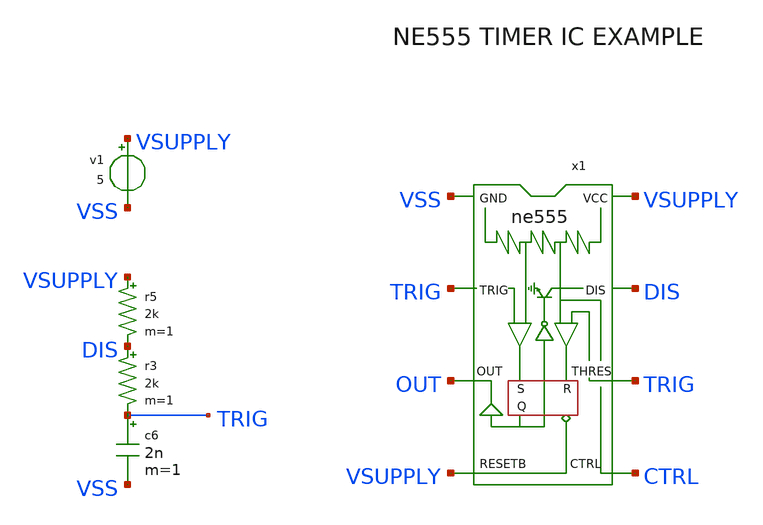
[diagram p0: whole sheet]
** sch_path: library/examples/test_ne555.sch
**.subckt test_ne555
x1 VSS TRIG OUT VSUPPLY CTRL TRIG DIS VSUPPLY ne555
r3 DIS TRIG 2k m=1
c6 TRIG VSS 2n m=1
v1 VSUPPLY VSS 5
r5 VSUPPLY DIS 2k m=1
**** begin user architecture code

.option SCALE=1e-6 PARHIER=LOCAL RUNLVL=6 post MODMONTE=1
.option sampling_method = SRS
* .option method=gear
vvss vss 0 dc 0

.temp 30
.tran 1n 1m uic


.MODEL bd139_2 npn IS=1e-09 BF=222.664 NF=0.85 VAF=36.4079 IKF=0.166126 ISE=5.03418e-09 NE=1.45313
+ BR=1.35467 NR=1.33751 VAR=142.931 IKR=1.66126 ISC=5.02557e-09 NC=3.10227 RB=26.9143 IRB=0.1 RBM=0.1
+ RE=0.000472454 RC=1.04109 XTB=0.727762 XTI=1.04311 EG=1.05 CJE=1e-11 VJE=0.75 MJE=0.33 TF=1e-09 XTF=1 VTF=10
+ ITF=0.01 CJC=1e-11 VJC=0.75 MJC=0.33 XCJC=0.9 FC=0.5 CJS=0 VJS=0.75 MJS=0.5 TR=1e-07 PTF=0 KF=0 AF=1


.MODEL BD139 NPN ( IS=2.3985E-13 mfg=Fairchild Vceo=80 Icrating=1500m BF=244.9 NF=1.0 BR=78.11
+ NR=1.007 ISE=1.0471E-14 NE=1.2 ISC=1.9314E-11 NC=1.45 VAF=98.5 VAR=7.46 IKF=1.1863 IKR=0.1445 RB=2.14
+ RBM=0.001 IRB=0.031 RE=0.0832 RC=0.01 CJE=2.92702E-10 VJE=0.67412 MJE=0.3300 FC=0.5 CJC=4.8831E-11 VJC=0.5258
+ MJC=0.3928 XCJC=0.5287 XTB=1.1398 EG=1.2105 XTI=3.0)

* sot-32
.MODEL bd237 npn IS=3.39253e-12 BF=108.002 NF=0.85 VAF=54.0829 IKF=1.0435 ISE=6.43245e-12 NE=3.3968
+ BR=4.46493 NR=0.843007 VAR=4.13248 IKR=3.42156 ISC=3.89999e-13 NC=3.99 RB=8.81471 IRB=0.1 RBM=0.1
+ RE=0.00101545 RC=0.282939 XTB=0.1 XTI=1 EG=1.206 CJE=6.77107e-08 VJE=0.559947 MJE=0.503582 TF=1e-08 XTF=1.35725
+ VTF=0.996034 ITF=0.999921 CJC=4.44295e-10 VJC=0.400232 MJC=0.41007 XCJC=0.803125 FC=0.598714 CJS=0 VJS=0.75
+ MJS=0.5 TR=1e-07 PTF=0 KF=0 AF=1

.MODEL Q2N2222A NPN IS =3.0611E-14 NF =1.00124 BF =220 IKF=0.52                VAF=104 ISE=7.5E-15
+ NE =1.41 NR =1.005 BR =4 IKR=0.24                VAR=28 ISC=1.06525E-11 NC =1.3728 RB =0.13 RE =0.22
+                RC =0.12 CJC=9.12E-12 MJC=0.3508 VJC=0.4089                CJE=27.01E-12 TF =0.325E-9 TR =100E-9

.MODEL Q2N2222 NPN      (          IS = 3.97589E-14          BF = 195.3412          NF = 1.0040078
+         VAF = 53.081         IKF = 0.976         ISE = 1.60241E-14          NE = 1.4791931          BR =
+ 1.1107942          NR = 0.9928261         VAR = 11.3571702         IKR = 2.4993953         ISC = 1.88505E-12
+          NC = 1.1838278          RB = 56.5826472         IRB = 1.50459E-4         RBM = 5.2592283          RE =
+ 0.0402974          RC = 0.4208         CJE = 2.56E-11         VJE = 0.682256         MJE = 0.3358856
+          TF = 3.3E-10         XTF = 6         VTF = 0.574         ITF = 0.32         PTF = 25.832         CJC =
+ 1.40625E-11         VJC = 0.5417393         MJC = 0.4547893        XCJC = 1          TR = 3.2E-7         CJS =
+ 0         VJS = .75         MJS = 0         XTB = 1.6486          EG = 1.11         XTI = 5.8315
+          KF = 0          AF = 1          FC = 0.83  )

.model D1N4007 D(IS=7.02767n RS=0.0341512 N=1.80803 EG=1.05743 XTI=5 BV=1000 IBV=5e-08 CJO=1e-11
+ VJ=0.7 M=0.5 FC=0.5 TT=1e-07 mfg=OnSemi type=silicon)


.MODEL D1N4148 D   IS = 4.352E-9   N = 1.906   BV = 110   IBV = 0.0001   RS = 0.6458   CJO =
+ 7.048E-13   VJ = 0.869   M = 0.03   FC = 0.5   TT = 3.48E-9

** param order
* 1: gnd
* 2: trig
* 3: out
* 4: reset#
* 5: ctrl
* 6: thres
* 7: dis
* 8: vcc
.SUBCKT ne555  34 32 30 19 23 33 1  21
*              G  TR O  R  F  TH D  V
Q4 25 2 3 QP
Q5 34 6 3 QP
Q6 6 6 8 QP
R1 9 21 4.7K
R2 3 21 830
R3 8 21 4.7K
Q7 2 33 5 QN
Q8 2 5 17 QN
Q9 6 4 17 QN
Q10 6 23 4 QN
Q11 12 20 10 QP
R4 10 21 1K
Q12 22 11 12 QP
Q13 14 13 12 QP
Q14 34 32 11 QP
Q15 14 18 13 QP
R5 14 34 100K
R6 22 34 100K
R7 17 34 10K
Q16 1 15 34 QN
Q17 15 19 31 QP
R8 18 23 5K
R9 18 34 5K
R10 21 23 5K
Q18 27 20 21 QP
Q19 20 20 21 QP
R11 20 31 5K
D1 31 24 DA
Q20 24 25 34 QN
Q21 25 22 34 QN
Q22 27 24 34 QN
R12 25 27 4.7K
R13 21 29 6.8K
Q23 21 29 28 QN
Q24 29 27 16 QN
Q25 30 26 34 QN
Q26 21 28 30 QN
D2 30 29 DA
R14 16 15 100
R15 16 26 220
R16 16 34 4.7K
R17 28 30 3.9K
Q3 2 2 9 QP
.MODEL DA D (RS=40 IS=1.0E-14 CJO=1PF)
.MODEL QP PNP (level=1 BF=20 BR=0.02 RC=4 RB=25 IS=1.0E-14 VA=50 NE=2)  CJE=12.4P VJE=1.1 MJE=.5
+ CJC=4.02P VJC=.3 MJC=.3 TF=229P TR=159N)
.MODEL QN NPN (level=1 IS=5.07F NF=1 BF=100 VAF=161 IKF=30M ISE=3.9P NE=2  BR=4 NR=1 VAR=16 IKR=45M
+ RE=1.03 RB=4.12 RC=.412 XTB=1.5  CJE=12.4P VJE=1.1 MJE=.5 CJC=4.02P VJC=.3 MJC=.3 TF=229P TR=959P)
.ENDS

**** end user architecture code
**.ends
.end
